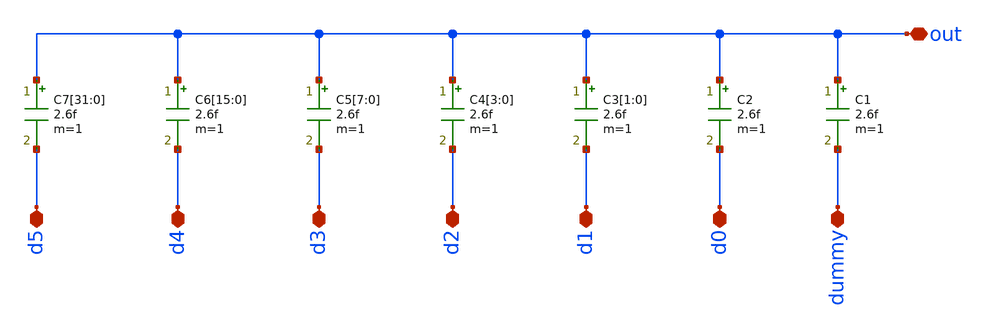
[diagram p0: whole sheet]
** sch_path: xschem/sar_10b/dac/carray2.sch
**.subckt carray2 out d5 d4 d2 d0 dummy d3 d1
*.iopin out
*.iopin d5
*.iopin d4
*.iopin d2
*.iopin d0
*.iopin dummy
*.iopin d3
*.iopin d1
C1 out dummy 2.6f m=1
C2 out d0 2.6f m=1
C3[1] out d1 2.6f m=1
C3[0] out d1 2.6f m=1
C4[3] out d2 2.6f m=1
C4[2] out d2 2.6f m=1
C4[1] out d2 2.6f m=1
C4[0] out d2 2.6f m=1
C5[7] out d3 2.6f m=1
C5[6] out d3 2.6f m=1
C5[5] out d3 2.6f m=1
C5[4] out d3 2.6f m=1
C5[3] out d3 2.6f m=1
C5[2] out d3 2.6f m=1
C5[1] out d3 2.6f m=1
C5[0] out d3 2.6f m=1
C6[15] out d4 2.6f m=1
C6[14] out d4 2.6f m=1
C6[13] out d4 2.6f m=1
C6[12] out d4 2.6f m=1
C6[11] out d4 2.6f m=1
C6[10] out d4 2.6f m=1
C6[9] out d4 2.6f m=1
C6[8] out d4 2.6f m=1
C6[7] out d4 2.6f m=1
C6[6] out d4 2.6f m=1
C6[5] out d4 2.6f m=1
C6[4] out d4 2.6f m=1
C6[3] out d4 2.6f m=1
C6[2] out d4 2.6f m=1
C6[1] out d4 2.6f m=1
C6[0] out d4 2.6f m=1
C7[31] out d5 2.6f m=1
C7[30] out d5 2.6f m=1
C7[29] out d5 2.6f m=1
C7[28] out d5 2.6f m=1
C7[27] out d5 2.6f m=1
C7[26] out d5 2.6f m=1
C7[25] out d5 2.6f m=1
C7[24] out d5 2.6f m=1
C7[23] out d5 2.6f m=1
C7[22] out d5 2.6f m=1
C7[21] out d5 2.6f m=1
C7[20] out d5 2.6f m=1
C7[19] out d5 2.6f m=1
C7[18] out d5 2.6f m=1
C7[17] out d5 2.6f m=1
C7[16] out d5 2.6f m=1
C7[15] out d5 2.6f m=1
C7[14] out d5 2.6f m=1
C7[13] out d5 2.6f m=1
C7[12] out d5 2.6f m=1
C7[11] out d5 2.6f m=1
C7[10] out d5 2.6f m=1
C7[9] out d5 2.6f m=1
C7[8] out d5 2.6f m=1
C7[7] out d5 2.6f m=1
C7[6] out d5 2.6f m=1
C7[5] out d5 2.6f m=1
C7[4] out d5 2.6f m=1
C7[3] out d5 2.6f m=1
C7[2] out d5 2.6f m=1
C7[1] out d5 2.6f m=1
C7[0] out d5 2.6f m=1
**.ends
.end
